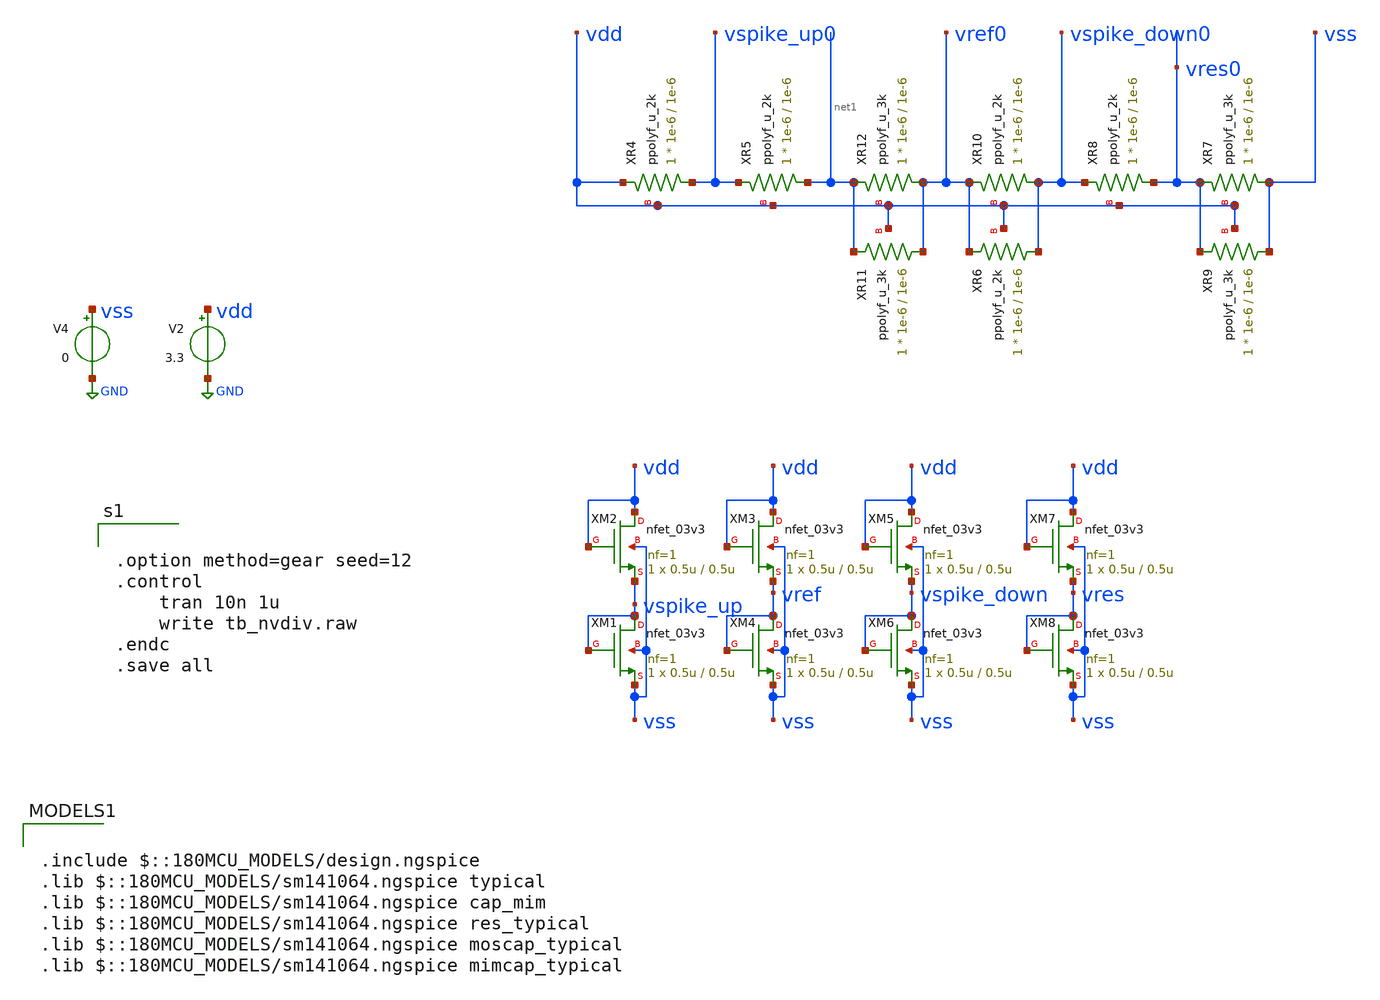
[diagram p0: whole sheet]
** sch_path: designs/libs/core_LIF_comp/tb_nvdiv/nvdiv.sch
**.subckt nvdiv
V2 vdd GND 3.3
V4 vss GND 0
XR4 vspike_up0 vdd vdd ppolyf_u_2k r_width=1e-6 r_length=1e-6 m=1
XR5 net1 vspike_up0 vdd ppolyf_u_2k r_width=1e-6 r_length=1e-6 m=1
XR6 vspike_down0 vref0 vdd ppolyf_u_2k r_width=1e-6 r_length=1e-6 m=1
XR8 vres0 vspike_down0 vdd ppolyf_u_2k r_width=1e-6 r_length=1e-6 m=1
XR9 vss vres0 vdd ppolyf_u_3k r_width=1e-6 r_length=1e-6 m=1
XR7 vss vres0 vdd ppolyf_u_3k r_width=1e-6 r_length=1e-6 m=1
XR10 vspike_down0 vref0 vdd ppolyf_u_2k r_width=1e-6 r_length=1e-6 m=1
XR12 vref0 net1 vdd ppolyf_u_3k r_width=1e-6 r_length=1e-6 m=1
XR11 vref0 net1 vdd ppolyf_u_3k r_width=1e-6 r_length=1e-6 m=1
XM2 vdd vdd vspike_up vss nfet_03v3 L=0.5u W=0.5u nf=1 ad='int((nf+1)/2) * W/nf * 0.18u' as='int((nf+2)/2) * W/nf * 0.18u'
+ pd='2*int((nf+1)/2) * (W/nf + 0.18u)' ps='2*int((nf+2)/2) * (W/nf + 0.18u)' nrd='0.18u / W' nrs='0.18u / W'
+ sa=0 sb=0 sd=0 m=1
XM1 vspike_up vspike_up vss vss nfet_03v3 L=0.5u W=0.5u nf=1 ad='int((nf+1)/2) * W/nf * 0.18u' as='int((nf+2)/2) * W/nf * 0.18u'
+ pd='2*int((nf+1)/2) * (W/nf + 0.18u)' ps='2*int((nf+2)/2) * (W/nf + 0.18u)' nrd='0.18u / W' nrs='0.18u / W'
+ sa=0 sb=0 sd=0 m=1
XM3 vdd vdd vref vss nfet_03v3 L=0.5u W=0.5u nf=1 ad='int((nf+1)/2) * W/nf * 0.18u' as='int((nf+2)/2) * W/nf * 0.18u'
+ pd='2*int((nf+1)/2) * (W/nf + 0.18u)' ps='2*int((nf+2)/2) * (W/nf + 0.18u)' nrd='0.18u / W' nrs='0.18u / W'
+ sa=0 sb=0 sd=0 m=1
XM4 vref vref vss vss nfet_03v3 L=0.5u W=0.5u nf=1 ad='int((nf+1)/2) * W/nf * 0.18u' as='int((nf+2)/2) * W/nf * 0.18u'
+ pd='2*int((nf+1)/2) * (W/nf + 0.18u)' ps='2*int((nf+2)/2) * (W/nf + 0.18u)' nrd='0.18u / W' nrs='0.18u / W'
+ sa=0 sb=0 sd=0 m=1
XM5 vdd vdd vspike_down vss nfet_03v3 L=0.5u W=0.5u nf=1 ad='int((nf+1)/2) * W/nf * 0.18u' as='int((nf+2)/2) * W/nf * 0.18u'
+ pd='2*int((nf+1)/2) * (W/nf + 0.18u)' ps='2*int((nf+2)/2) * (W/nf + 0.18u)' nrd='0.18u / W' nrs='0.18u / W'
+ sa=0 sb=0 sd=0 m=1
XM6 vspike_down vspike_down vss vss nfet_03v3 L=0.5u W=0.5u nf=1 ad='int((nf+1)/2) * W/nf * 0.18u' as='int((nf+2)/2) * W/nf * 0.18u'
+ pd='2*int((nf+1)/2) * (W/nf + 0.18u)' ps='2*int((nf+2)/2) * (W/nf + 0.18u)' nrd='0.18u / W' nrs='0.18u / W'
+ sa=0 sb=0 sd=0 m=1
XM7 vdd vdd vres vss nfet_03v3 L=0.5u W=0.5u nf=1 ad='int((nf+1)/2) * W/nf * 0.18u' as='int((nf+2)/2) * W/nf * 0.18u'
+ pd='2*int((nf+1)/2) * (W/nf + 0.18u)' ps='2*int((nf+2)/2) * (W/nf + 0.18u)' nrd='0.18u / W' nrs='0.18u / W'
+ sa=0 sb=0 sd=0 m=1
XM8 vres vres vss vss nfet_03v3 L=0.5u W=0.5u nf=1 ad='int((nf+1)/2) * W/nf * 0.18u' as='int((nf+2)/2) * W/nf * 0.18u'
+ pd='2*int((nf+1)/2) * (W/nf + 0.18u)' ps='2*int((nf+2)/2) * (W/nf + 0.18u)' nrd='0.18u / W' nrs='0.18u / W'
+ sa=0 sb=0 sd=0 m=1
**** begin user architecture code


.option method=gear seed=12
.control
    tran 10n 1u
    write tb_nvdiv.raw
.endc
.save all



.include $::180MCU_MODELS/design.ngspice
.lib $::180MCU_MODELS/sm141064.ngspice typical
.lib $::180MCU_MODELS/sm141064.ngspice cap_mim
.lib $::180MCU_MODELS/sm141064.ngspice res_typical
.lib $::180MCU_MODELS/sm141064.ngspice moscap_typical
.lib $::180MCU_MODELS/sm141064.ngspice mimcap_typical

**** end user architecture code
**.ends
.GLOBAL GND
.end
